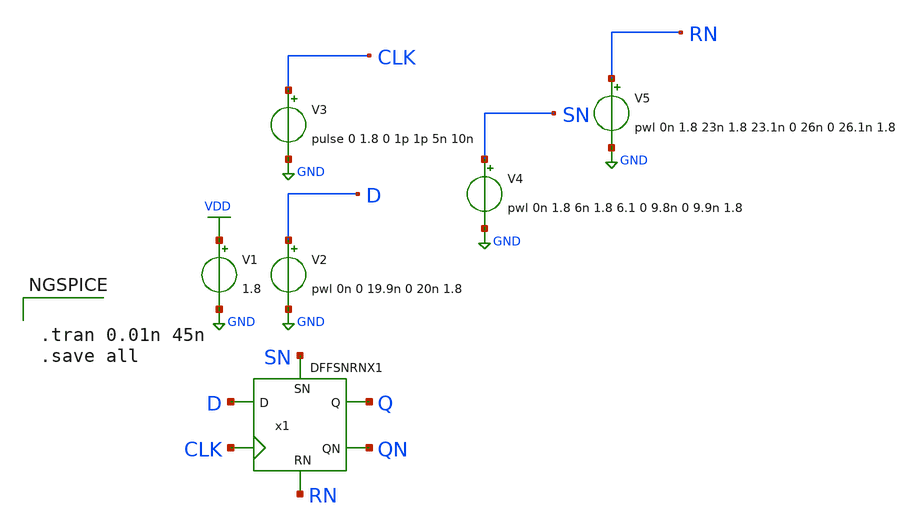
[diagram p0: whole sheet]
** sch_path: lib/xschem/test_DFFSNRNX1.sch
**.subckt test_DFFSNRNX1
V2 D GND pwl 0n 0 19.9n 0 20n 1.8
V1 VDD GND 1.8
V3 CLK GND pulse 0 1.8 0 1p 1p 5n 10n
V4 SN GND pwl 0n 1.8 6n 1.8 6.1 0 9.8n 0 9.9n 1.8
V5 RN GND pwl 0n 1.8 23n 1.8 23.1n 0 26n 0 26.1n 1.8
x1 Q QN D CLK SN RN VDD GND DFFSNRNX1
**** begin user architecture code

.lib $::SKYWATER_MODELS/sky130.lib.spice tt


**** end user architecture code
**.ends

* expanding   symbol:  DFFSNRNX1.sym # of pins=6
** sym_path: DFFSNRNX1.sym
** sch_path: DFFSNRNX1.sch
.subckt DFFSNRNX1 Q QN D CLK SN RN VDD VSS
*.ipin D
*.opin QN
*.ipin SN
*.ipin CLK
*.opin Q
*.ipin RN
x3 net3 net1 SN net4 NAND3X1
x2 net2 net1 CLK net4 NAND3X1
x6 Q QN SN net4 NAND3X1
x1 net1 D RN net2 NAND3X1
x4 net4 net3 CLK RN NAND3X1
x5 QN net2 RN Q NAND3X1
.ends


* expanding   symbol:  NAND3X1.sym # of pins=4
** sym_path: lib/xschem/NAND3X1.sym
** sch_path: lib/xschem/NAND3X1.sch
.subckt NAND3X1 Y A B C
*.ipin A
*.opin Y
*.ipin B
*.ipin C
XM1 net2 C GND GND sky130_fd_pr__nfet_01v8 L=0.15 W=3 nf=1 ad='int((nf+1)/2) * W/nf * 0.29' as='int((nf+2)/2) * W/nf * 0.29'
+ pd='2*int((nf+1)/2) * (W/nf + 0.29)' ps='2*int((nf+2)/2) * (W/nf + 0.29)' nrd='0.29 / W' nrs='0.29 / W'
+ sa=0 sb=0 sd=0 mult=1 m=1
XM2 Y A VDD VDD sky130_fd_pr__pfet_01v8 L=0.15 W=2 nf=1 ad='int((nf+1)/2) * W/nf * 0.29' as='int((nf+2)/2) * W/nf * 0.29'
+ pd='2*int((nf+1)/2) * (W/nf + 0.29)' ps='2*int((nf+2)/2) * (W/nf + 0.29)' nrd='0.29 / W' nrs='0.29 / W'
+ sa=0 sb=0 sd=0 mult=1 m=1
XM3 net1 B net2 GND sky130_fd_pr__nfet_01v8 L=0.15 W=3 nf=1 ad='int((nf+1)/2) * W/nf * 0.29' as='int((nf+2)/2) * W/nf * 0.29'
+ pd='2*int((nf+1)/2) * (W/nf + 0.29)' ps='2*int((nf+2)/2) * (W/nf + 0.29)' nrd='0.29 / W' nrs='0.29 / W'
+ sa=0 sb=0 sd=0 mult=1 m=1
XM4 Y A net1 GND sky130_fd_pr__nfet_01v8 L=0.15 W=3 nf=1 ad='int((nf+1)/2) * W/nf * 0.29' as='int((nf+2)/2) * W/nf * 0.29'
+ pd='2*int((nf+1)/2) * (W/nf + 0.29)' ps='2*int((nf+2)/2) * (W/nf + 0.29)' nrd='0.29 / W' nrs='0.29 / W'
+ sa=0 sb=0 sd=0 mult=1 m=1
XM5 Y A VDD VDD sky130_fd_pr__pfet_01v8 L=0.15 W=2 nf=1 ad='int((nf+1)/2) * W/nf * 0.29' as='int((nf+2)/2) * W/nf * 0.29'
+ pd='2*int((nf+1)/2) * (W/nf + 0.29)' ps='2*int((nf+2)/2) * (W/nf + 0.29)' nrd='0.29 / W' nrs='0.29 / W'
+ sa=0 sb=0 sd=0 mult=1 m=1
XM6 Y B VDD VDD sky130_fd_pr__pfet_01v8 L=0.15 W=2 nf=1 ad='int((nf+1)/2) * W/nf * 0.29' as='int((nf+2)/2) * W/nf * 0.29'
+ pd='2*int((nf+1)/2) * (W/nf + 0.29)' ps='2*int((nf+2)/2) * (W/nf + 0.29)' nrd='0.29 / W' nrs='0.29 / W'
+ sa=0 sb=0 sd=0 mult=1 m=1
XM7 Y B VDD VDD sky130_fd_pr__pfet_01v8 L=0.15 W=2 nf=1 ad='int((nf+1)/2) * W/nf * 0.29' as='int((nf+2)/2) * W/nf * 0.29'
+ pd='2*int((nf+1)/2) * (W/nf + 0.29)' ps='2*int((nf+2)/2) * (W/nf + 0.29)' nrd='0.29 / W' nrs='0.29 / W'
+ sa=0 sb=0 sd=0 mult=1 m=1
XM8 Y C VDD VDD sky130_fd_pr__pfet_01v8 L=0.15 W=2 nf=1 ad='int((nf+1)/2) * W/nf * 0.29' as='int((nf+2)/2) * W/nf * 0.29'
+ pd='2*int((nf+1)/2) * (W/nf + 0.29)' ps='2*int((nf+2)/2) * (W/nf + 0.29)' nrd='0.29 / W' nrs='0.29 / W'
+ sa=0 sb=0 sd=0 mult=1 m=1
XM9 Y C VDD VDD sky130_fd_pr__pfet_01v8 L=0.15 W=2 nf=1 ad='int((nf+1)/2) * W/nf * 0.29' as='int((nf+2)/2) * W/nf * 0.29'
+ pd='2*int((nf+1)/2) * (W/nf + 0.29)' ps='2*int((nf+2)/2) * (W/nf + 0.29)' nrd='0.29 / W' nrs='0.29 / W'
+ sa=0 sb=0 sd=0 mult=1 m=1
.ends

.GLOBAL VDD
.GLOBAL GND
**** begin user architecture code


.tran 0.01n 45n
.save all


**** end user architecture code
.end
